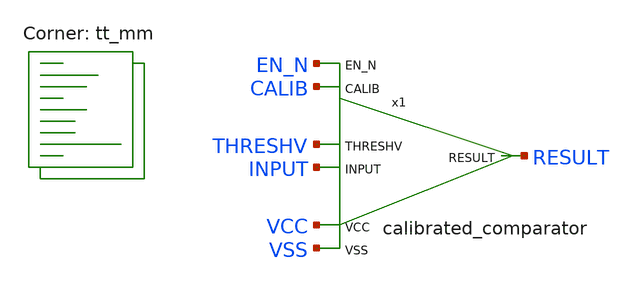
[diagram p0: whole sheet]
** sch_path: xschem/tb_calibrated_comparator.sch
**.subckt tb_calibrated_comparator
x1 VCC VSS INPUT THRESHV RESULT CALIB EN_N calibrated_comparator
**** begin user architecture code
.lib $::SKYWATER_MODELS/sky130.lib.spice tt_mm


** this experimental option enables mos model bin
** selection based on W/NF instead of W
.option chgtol=4e-16 method=gear

.param VCCGAUSS = agauss(1.8, 0.05, 1)
.param VCC = 'VCCGAUSS'
** use following line to remove VCC variations
* .param VCC = 1.8
.param VDLGAUSS = agauss(0.9, 0.23, 1)
.param VDL = VDLGAUSS
** use following line to remove input common mode variations
* .param VDL =  0.9
.param TEMPGAUSS = agauss(40, 30, 1)
.option temp = 'TEMPGAUSS'
** use following line to remove temperature variations
* .option temp = 25
.param DELTA = 0.002

.include stimuli_tb_calibrated_comparator.cir

.control
  setseed  8
  reset
  let run = 1
  save all
  op
  write tb_calibrated_comparator.raw
  reset
  set appendwrite
  dowhile run < = 5
    save all
    tran 1n 3200n uic
    write tb_calibrated_comparator.raw
    let run = run + 1
    reset
  end
  quit 0
.endc


**** end user architecture code
**.ends
.end
